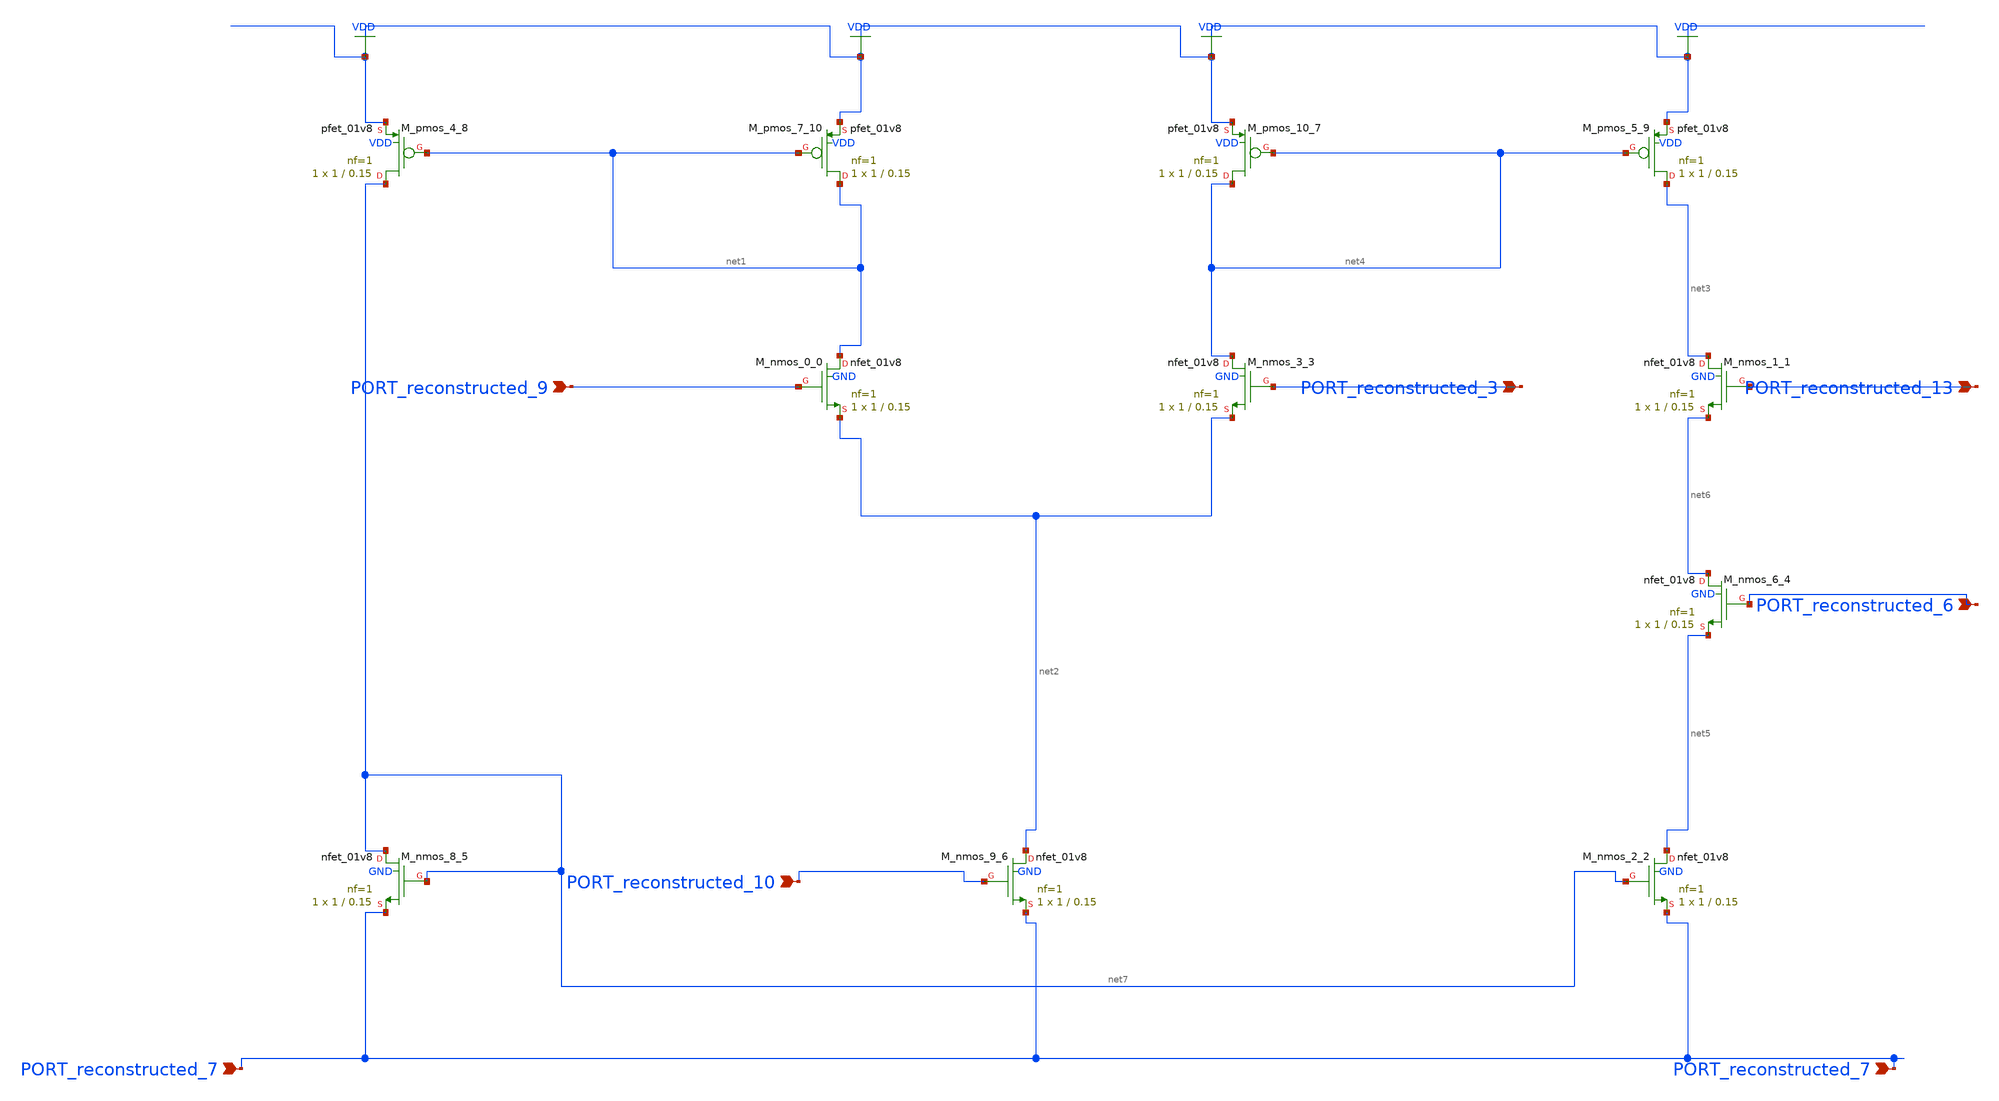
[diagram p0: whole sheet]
** sch_path: schematics/SchemGen/10_11591_ijece_v12i2_pp2158-2168_04_001_canvas.sch
**.subckt 10_11591_ijece_v12i2_pp2158-2168_04_001_canvas PORT_reconstructed_10 PORT_reconstructed_6
*+ PORT_reconstructed_9 PORT_reconstructed_13 PORT_reconstructed_3 PORT_reconstructed_7 PORT_reconstructed_7
*.ipin PORT_reconstructed_10
*.ipin PORT_reconstructed_6
*.ipin PORT_reconstructed_9
*.ipin PORT_reconstructed_13
*.ipin PORT_reconstructed_3
*.ipin PORT_reconstructed_7
*.ipin PORT_reconstructed_7
XM_nmos_0_0 net1 PORT_reconstructed_9 net2 GND sky130_fd_pr__nfet_01v8 L=0.15 W=1 nf=1 ad='int((1 + 1)/2) * 1 / 1 * 0.29'
+ as='int((1 + 2)/2) * 1 / 1 * 0.29' pd='2*int((1 + 1)/2) * (1 / 1 + 0.29)' ps='2*int((1 + 2)/2) * (1 / 1 + 0.29)'
+ nrd='0.29 / 1 ' nrs='0.29 / 1 ' sa=0 sb=0 sd=0 mult=1 m=1
XM_nmos_1_1 net3 PORT_reconstructed_13 net6 GND sky130_fd_pr__nfet_01v8 L=0.15 W=1 nf=1 ad='int((1 + 1)/2) * 1 / 1 * 0.29'
+ as='int((1 + 2)/2) * 1 / 1 * 0.29' pd='2*int((1 + 1)/2) * (1 / 1 + 0.29)' ps='2*int((1 + 2)/2) * (1 / 1 + 0.29)'
+ nrd='0.29 / 1 ' nrs='0.29 / 1 ' sa=0 sb=0 sd=0 mult=1 m=1
XM_nmos_2_2 net5 net7 PORT_reconstructed_7 GND sky130_fd_pr__nfet_01v8 L=0.15 W=1 nf=1 ad='int((1 + 1)/2) * 1 / 1 * 0.29'
+ as='int((1 + 2)/2) * 1 / 1 * 0.29' pd='2*int((1 + 1)/2) * (1 / 1 + 0.29)' ps='2*int((1 + 2)/2) * (1 / 1 + 0.29)'
+ nrd='0.29 / 1 ' nrs='0.29 / 1 ' sa=0 sb=0 sd=0 mult=1 m=1
XM_nmos_3_3 net4 PORT_reconstructed_3 net2 GND sky130_fd_pr__nfet_01v8 L=0.15 W=1 nf=1 ad='int((1 + 1)/2) * 1 / 1 * 0.29'
+ as='int((1 + 2)/2) * 1 / 1 * 0.29' pd='2*int((1 + 1)/2) * (1 / 1 + 0.29)' ps='2*int((1 + 2)/2) * (1 / 1 + 0.29)'
+ nrd='0.29 / 1 ' nrs='0.29 / 1 ' sa=0 sb=0 sd=0 mult=1 m=1
XM_nmos_6_4 net6 PORT_reconstructed_6 net5 GND sky130_fd_pr__nfet_01v8 L=0.15 W=1 nf=1 ad='int((1 + 1)/2) * 1 / 1 * 0.29'
+ as='int((1 + 2)/2) * 1 / 1 * 0.29' pd='2*int((1 + 1)/2) * (1 / 1 + 0.29)' ps='2*int((1 + 2)/2) * (1 / 1 + 0.29)'
+ nrd='0.29 / 1 ' nrs='0.29 / 1 ' sa=0 sb=0 sd=0 mult=1 m=1
XM_nmos_8_5 net7 net7 PORT_reconstructed_7 GND sky130_fd_pr__nfet_01v8 L=0.15 W=1 nf=1 ad='int((1 + 1)/2) * 1 / 1 * 0.29'
+ as='int((1 + 2)/2) * 1 / 1 * 0.29' pd='2*int((1 + 1)/2) * (1 / 1 + 0.29)' ps='2*int((1 + 2)/2) * (1 / 1 + 0.29)'
+ nrd='0.29 / 1 ' nrs='0.29 / 1 ' sa=0 sb=0 sd=0 mult=1 m=1
XM_nmos_9_6 net2 PORT_reconstructed_10 PORT_reconstructed_7 GND sky130_fd_pr__nfet_01v8 L=0.15 W=1 nf=1
+ ad='int((1 + 1)/2) * 1 / 1 * 0.29' as='int((1 + 2)/2) * 1 / 1 * 0.29' pd='2*int((1 + 1)/2) * (1 / 1 + 0.29)'
+ ps='2*int((1 + 2)/2) * (1 / 1 + 0.29)' nrd='0.29 / 1 ' nrs='0.29 / 1 ' sa=0 sb=0 sd=0 mult=1 m=1
XM_pmos_10_7 net4 net4 VDD VDD sky130_fd_pr__pfet_01v8 L=0.15 W=1 nf=1 ad='int((1 + 1)/2) * 1 / 1 * 0.29'
+ as='int((1 + 2)/2) * 1 / 1 * 0.29' pd='2*int((1 + 1)/2) * (1 / 1 + 0.29)' ps='2*int((1 + 2)/2) * (1 / 1 + 0.29)'
+ nrd='0.29 / 1 ' nrs='0.29 / 1 ' sa=0 sb=0 sd=0 mult=1 m=1
XM_pmos_4_8 net7 net1 VDD VDD sky130_fd_pr__pfet_01v8 L=0.15 W=1 nf=1 ad='int((1 + 1)/2) * 1 / 1 * 0.29'
+ as='int((1 + 2)/2) * 1 / 1 * 0.29' pd='2*int((1 + 1)/2) * (1 / 1 + 0.29)' ps='2*int((1 + 2)/2) * (1 / 1 + 0.29)'
+ nrd='0.29 / 1 ' nrs='0.29 / 1 ' sa=0 sb=0 sd=0 mult=1 m=1
XM_pmos_5_9 net3 net4 VDD VDD sky130_fd_pr__pfet_01v8 L=0.15 W=1 nf=1 ad='int((1 + 1)/2) * 1 / 1 * 0.29'
+ as='int((1 + 2)/2) * 1 / 1 * 0.29' pd='2*int((1 + 1)/2) * (1 / 1 + 0.29)' ps='2*int((1 + 2)/2) * (1 / 1 + 0.29)'
+ nrd='0.29 / 1 ' nrs='0.29 / 1 ' sa=0 sb=0 sd=0 mult=1 m=1
XM_pmos_7_10 net1 net1 VDD VDD sky130_fd_pr__pfet_01v8 L=0.15 W=1 nf=1 ad='int((1 + 1)/2) * 1 / 1 * 0.29'
+ as='int((1 + 2)/2) * 1 / 1 * 0.29' pd='2*int((1 + 1)/2) * (1 / 1 + 0.29)' ps='2*int((1 + 2)/2) * (1 / 1 + 0.29)'
+ nrd='0.29 / 1 ' nrs='0.29 / 1 ' sa=0 sb=0 sd=0 mult=1 m=1
**.ends
.GLOBAL VDD
.end
